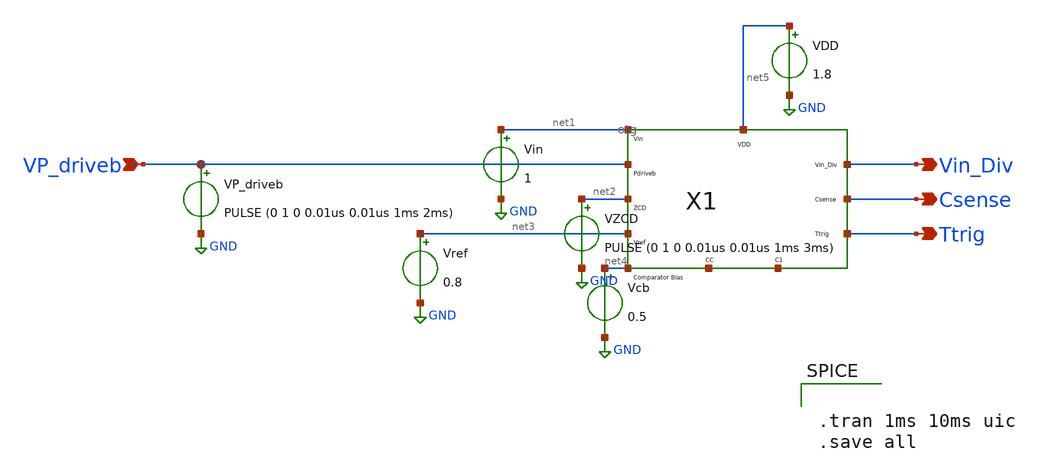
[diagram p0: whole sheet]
** sch_path: Current Sensor/otg_testing.sch
**.subckt otg_testing Vin_Div Csense Ttrig VP_driveb
*.opin Vin_Div
*.opin Csense
*.opin Ttrig
*.ipin VP_driveb
X1 net1 VP_driveb net2 net3 net4 net5 Vin_Div Csense Ttrig net6 net7 otg
Vin net1 GND 1
Vref net3 GND 0.8
VDD net5 GND 1.8
Vcb net4 GND 0.5
VP_driveb VP_driveb GND PULSE (0 1 0 0.01us 0.01us 1ms 2ms)
VZCD net2 GND PULSE (0 1 0 0.01us 0.01us 1ms 3ms)
**** begin user architecture code


.tran 1ms 10ms uic
.save all


** opencircuitdesign pdks install
.lib $::SKYWATER_MODELS/sky130.lib.spice tt_mm


**** end user architecture code
**.ends
.GLOBAL GND
.end
